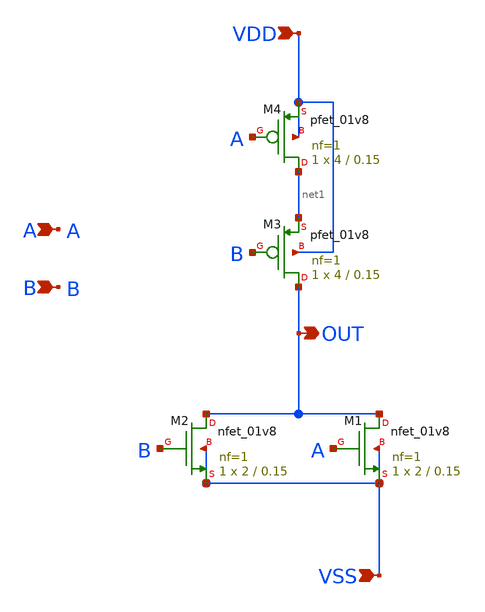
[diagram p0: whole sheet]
** sch_path: design/LELO_SVOD_SKY130A/LELO_NOR.sch
**.subckt LELO_NOR VDD VSS OUT A B
*.ipin VDD
*.ipin VSS
*.opin OUT
*.ipin A
*.ipin B
XM2 OUT B VSS VSS sky130_fd_pr__nfet_01v8 L=0.15 W=2 nf=1 ad='int((1 + 1)/2) * 2 / 1 * 0.29' as='int((1 + 2)/2) * 2 / 1 * 0.29'
+ pd='2*int((1 + 1)/2) * (2 / 1 + 0.29)' ps='2*int((1 + 2)/2) * (2 / 1 + 0.29)' nrd='0.29 / 2 ' nrs='0.29 / 2 '
+ sa=0 sb=0 sd=0 mult=1 m=1
XM1 OUT A VSS VSS sky130_fd_pr__nfet_01v8 L=0.15 W=2 nf=1 ad='int((1 + 1)/2) * 2 / 1 * 0.29' as='int((1 + 2)/2) * 2 / 1 * 0.29'
+ pd='2*int((1 + 1)/2) * (2 / 1 + 0.29)' ps='2*int((1 + 2)/2) * (2 / 1 + 0.29)' nrd='0.29 / 2 ' nrs='0.29 / 2 '
+ sa=0 sb=0 sd=0 mult=1 m=1
XM3 OUT B net1 VDD sky130_fd_pr__pfet_01v8 L=0.15 W=4 nf=1 ad='int((1 + 1)/2) * 4 / 1 * 0.29' as='int((1 + 2)/2) * 4 / 1 * 0.29'
+ pd='2*int((1 + 1)/2) * (4 / 1 + 0.29)' ps='2*int((1 + 2)/2) * (4 / 1 + 0.29)' nrd='0.29 / 4 ' nrs='0.29 / 4 '
+ sa=0 sb=0 sd=0 mult=1 m=1
XM4 net1 A VDD VDD sky130_fd_pr__pfet_01v8 L=0.15 W=4 nf=1 ad='int((1 + 1)/2) * 4 / 1 * 0.29' as='int((1 + 2)/2) * 4 / 1 * 0.29'
+ pd='2*int((1 + 1)/2) * (4 / 1 + 0.29)' ps='2*int((1 + 2)/2) * (4 / 1 + 0.29)' nrd='0.29 / 4 ' nrs='0.29 / 4 '
+ sa=0 sb=0 sd=0 mult=1 m=1
**.ends
.end
